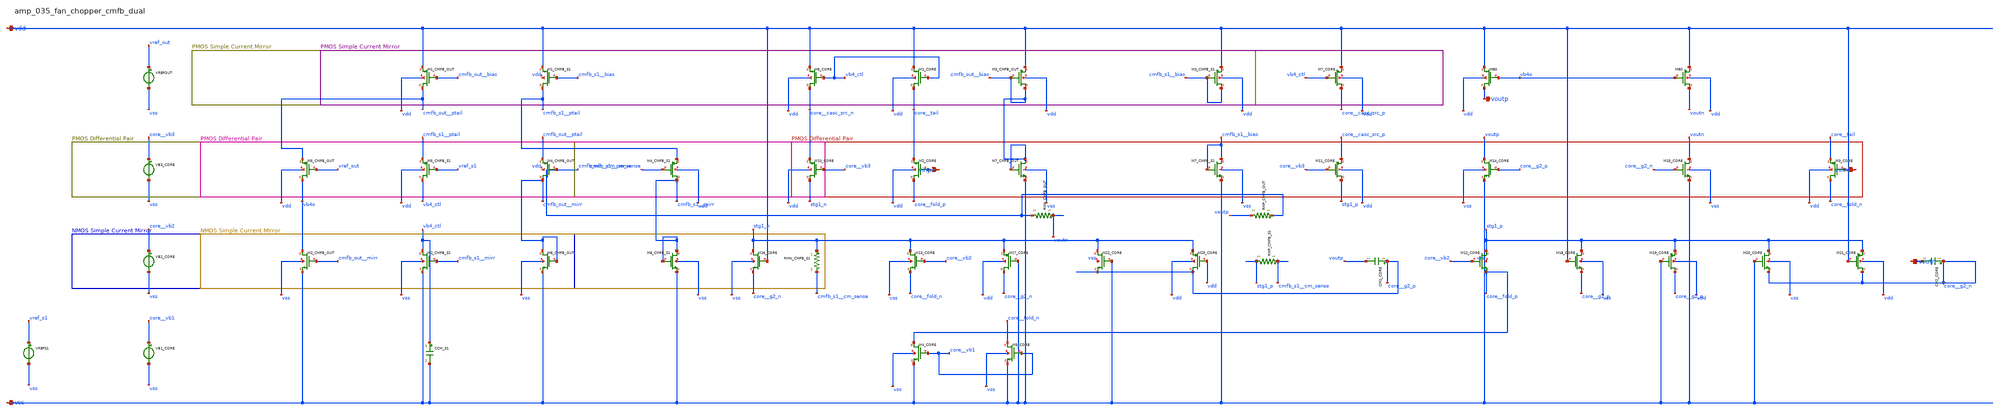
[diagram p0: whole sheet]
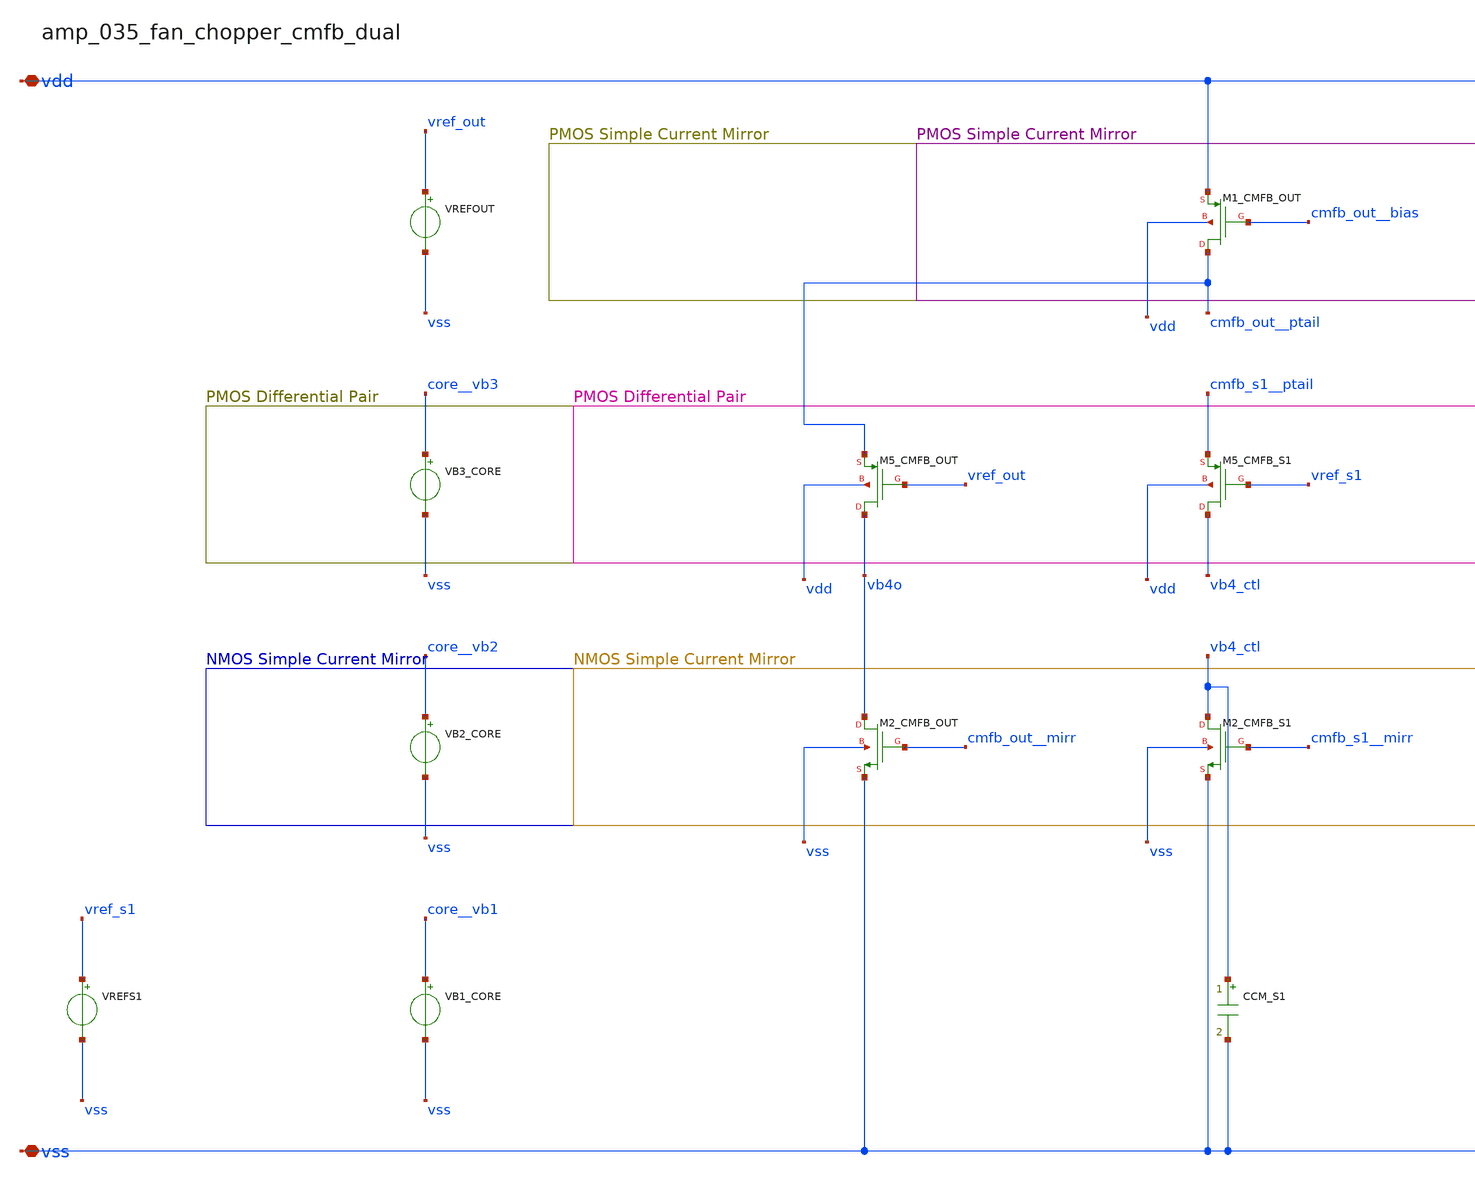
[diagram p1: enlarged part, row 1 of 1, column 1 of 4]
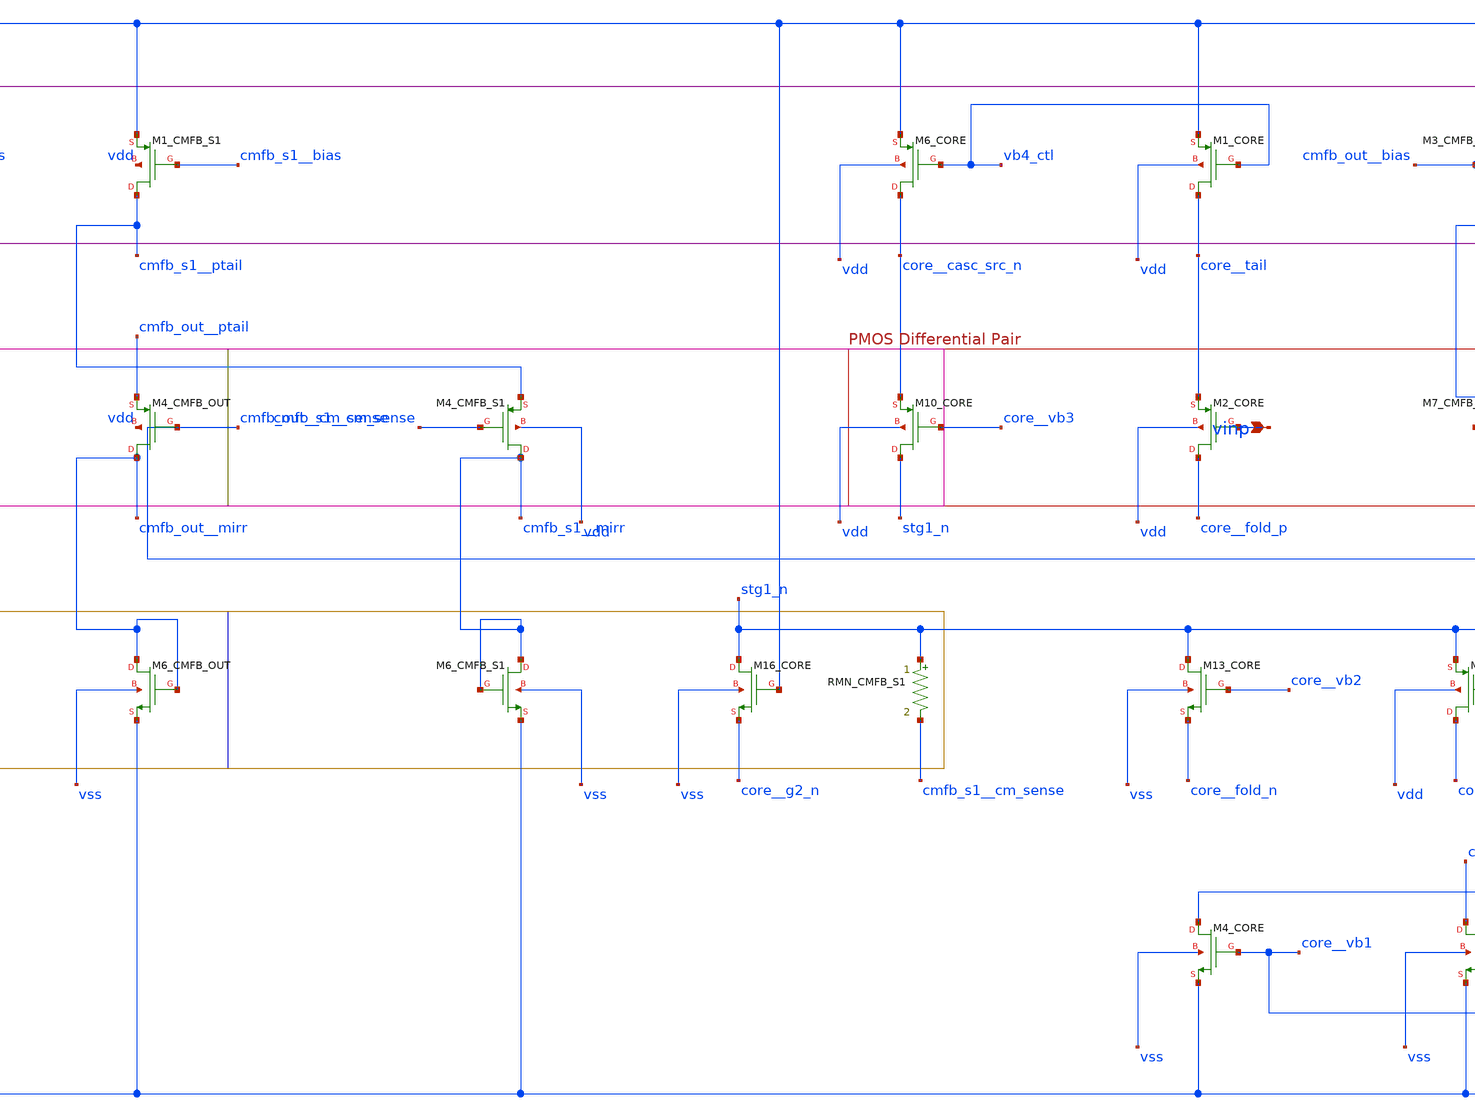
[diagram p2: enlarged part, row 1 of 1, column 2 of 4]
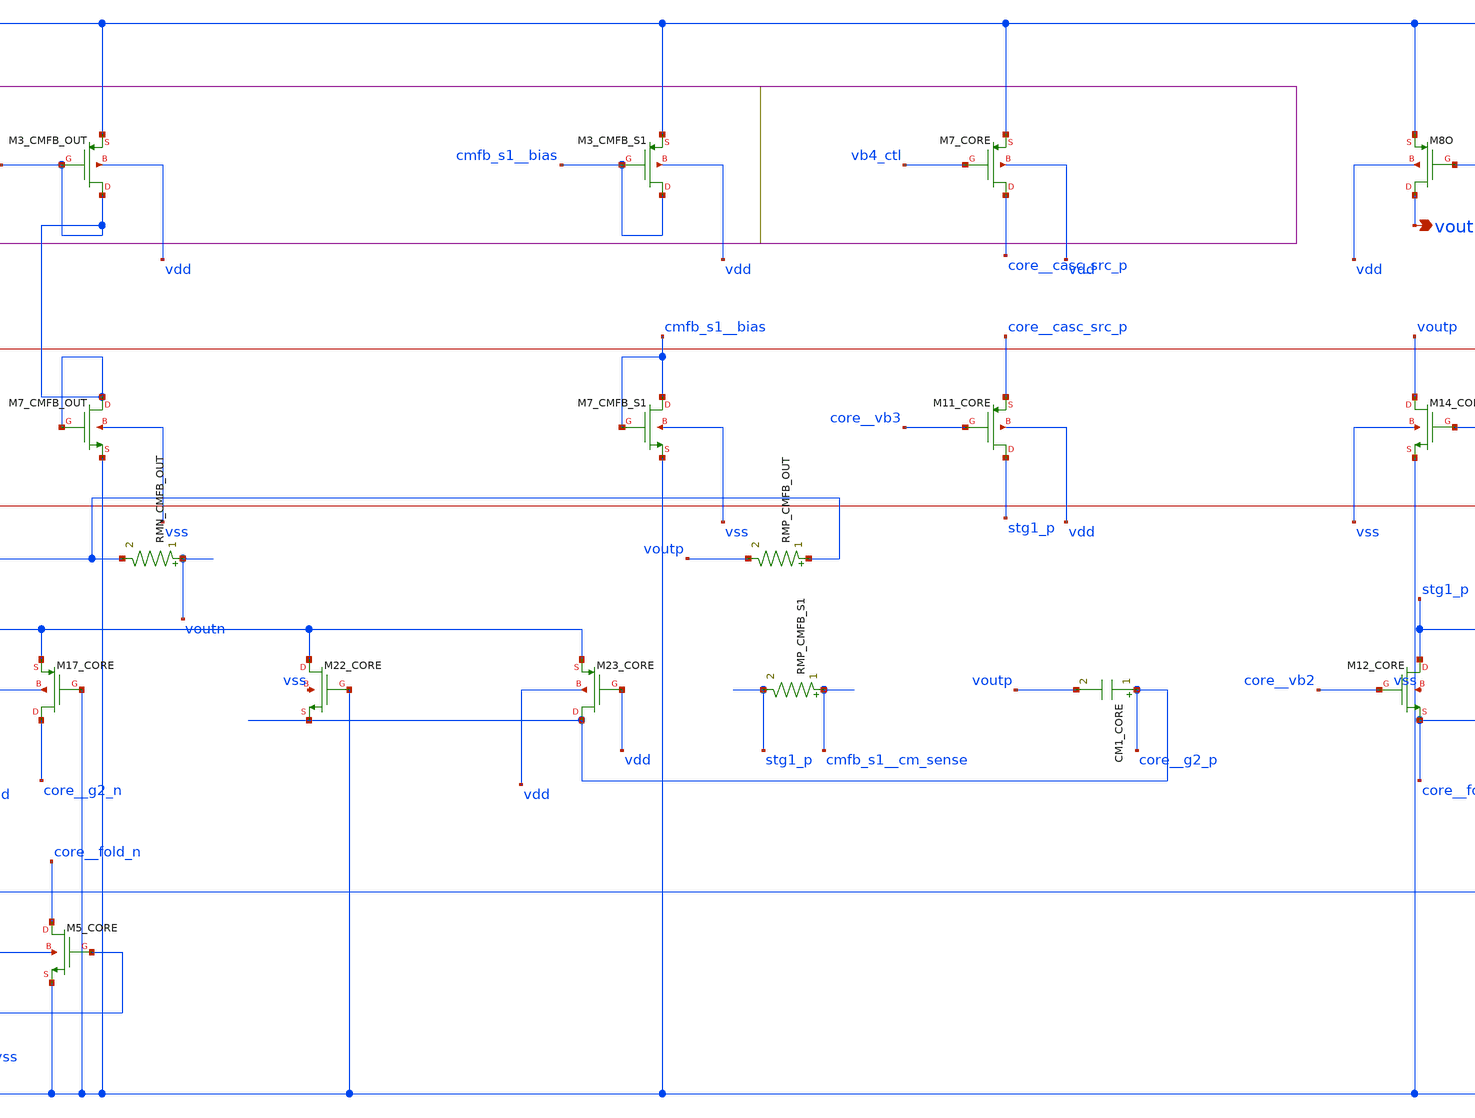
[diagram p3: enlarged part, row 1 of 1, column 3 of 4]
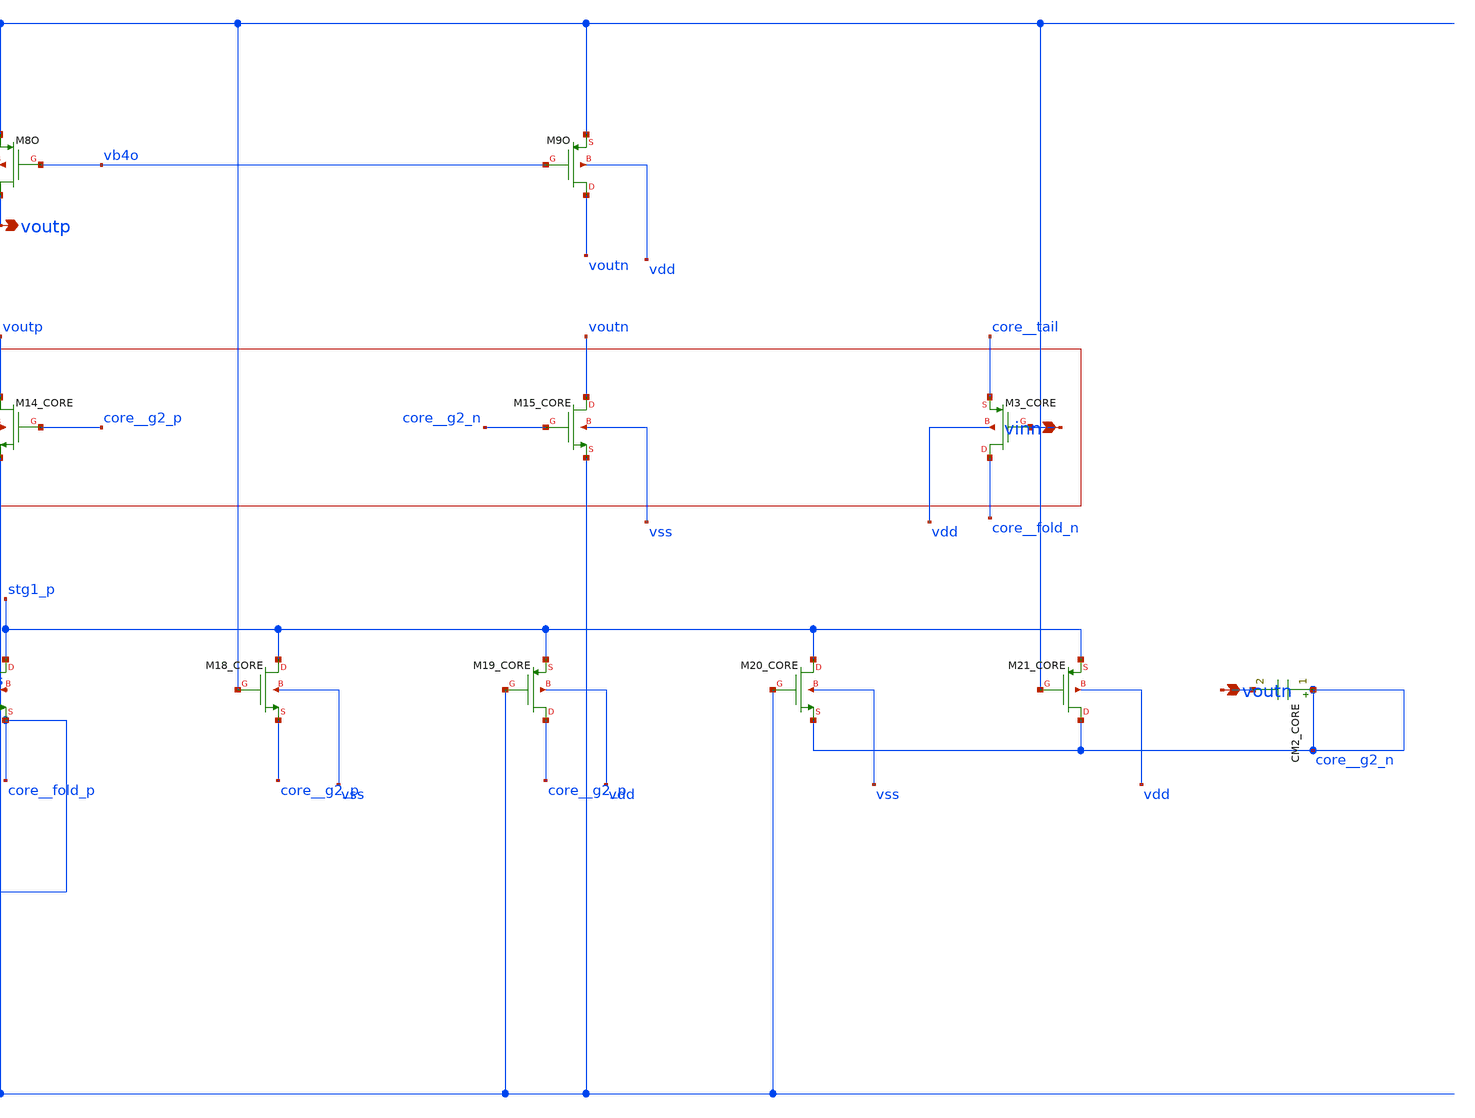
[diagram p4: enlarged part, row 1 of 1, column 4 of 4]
** sch_path: analog-db/raw/amp_035_fan_chopper_cmfb_dual/amp_035_fan_chopper_cmfb_dual_annotated.sch
**.subckt amp_035_fan_chopper_cmfb_dual_annotated vinp vinn vdd vss voutp voutn
*.ipin vinp
*.ipin vinn
*.iopin vdd
*.iopin vss
*.opin voutp
*.opin voutn
CCM_S1 vb4_ctl vss 'c_cm_s1' m=1
CM1_CORE core__g2_p voutp 'x_dut_cm1_core_value' m=1
CM2_CORE core__g2_n voutn 'x_dut_cm2_core_value' m=1
RMN_CMFB_OUT voutn cmfb_out__cm_sense 'x_dut_rmn_cmfb_out_value' m=1
RMN_CMFB_S1 stg1_n cmfb_s1__cm_sense 'x_dut_rmn_cmfb_s1_value' m=1
RMP_CMFB_OUT cmfb_out__cm_sense voutp 'x_dut_rmp_cmfb_out_value' m=1
RMP_CMFB_S1 cmfb_s1__cm_sense stg1_p 'x_dut_rmp_cmfb_s1_value' m=1
VB1_CORE core__vb1 vss dc {vb1_core}
VB2_CORE core__vb2 vss dc {vb2_core}
VB3_CORE core__vb3 vss dc {vb3_core}
VREFOUT vref_out vss dc {vcm_ref}
VREFS1 vref_s1 vss dc {vcm_ref_stg1}
XM10_CORE stg1_n core__vb3 core__casc_src_n vdd sg13_lv_pmos w=x_dut_xm10_core_w l=x_dut_xm10_core_l
+ ng=1 m=x_dut_xm10_core_m
XM11_CORE stg1_p core__vb3 core__casc_src_p vdd sg13_lv_pmos w=x_dut_xm11_core_w l=x_dut_xm11_core_l
+ ng=1 m=x_dut_xm11_core_m
XM12_CORE stg1_p core__vb2 core__fold_p vss sg13_lv_nmos w=x_dut_xm12_core_w l=x_dut_xm12_core_l
+ ng=1 m=x_dut_xm12_core_m
XM13_CORE stg1_n core__vb2 core__fold_n vss sg13_lv_nmos w=x_dut_xm13_core_w l=x_dut_xm13_core_l
+ ng=1 m=x_dut_xm13_core_m
XM14_CORE voutp core__g2_p vss vss sg13_lv_nmos w=x_dut_xm14_core_w l=x_dut_xm14_core_l ng=1
+ m=x_dut_xm14_core_m
XM15_CORE voutn core__g2_n vss vss sg13_lv_nmos w=x_dut_xm15_core_w l=x_dut_xm15_core_l ng=1
+ m=x_dut_xm15_core_m
XM16_CORE stg1_n vdd core__g2_n vss sg13_lv_nmos w=x_dut_xm16_core_w l=x_dut_xm16_core_l ng=1
+ m=x_dut_xm16_core_m
XM17_CORE core__g2_n vss stg1_n vdd sg13_lv_pmos w=x_dut_xm17_core_w l=x_dut_xm17_core_l ng=1
+ m=x_dut_xm17_core_m
XM18_CORE stg1_p vdd core__g2_p vss sg13_lv_nmos w=x_dut_xm18_core_w l=x_dut_xm18_core_l ng=1
+ m=x_dut_xm18_core_m
XM19_CORE core__g2_p vss stg1_p vdd sg13_lv_pmos w=x_dut_xm19_core_w l=x_dut_xm19_core_l ng=1
+ m=x_dut_xm19_core_m
XM1_CMFB_OUT cmfb_out__ptail cmfb_out__bias vdd vdd sg13_lv_pmos w=x_dut_xm1_cmfb_out_w
+ l=x_dut_xm1_cmfb_out_l ng=1 m=x_dut_xm1_cmfb_out_m
XM1_CMFB_S1 cmfb_s1__ptail cmfb_s1__bias vdd vdd sg13_lv_pmos w=x_dut_xm1_cmfb_s1_w
+ l=x_dut_xm1_cmfb_s1_l ng=1 m=x_dut_xm1_cmfb_s1_m
XM1_CORE core__tail vb4_ctl vdd vdd sg13_lv_pmos w=x_dut_xm1_core_w l=x_dut_xm1_core_l ng=1
+ m=x_dut_xm1_core_m
XM20_CORE stg1_p vss core__g2_n vss sg13_lv_nmos w=x_dut_xm20_core_w l=x_dut_xm20_core_l ng=1
+ m=x_dut_xm20_core_m
XM21_CORE core__g2_n vdd stg1_p vdd sg13_lv_pmos w=x_dut_xm21_core_w l=x_dut_xm21_core_l ng=1
+ m=x_dut_xm21_core_m
XM22_CORE stg1_n vss core__g2_p vss sg13_lv_nmos w=x_dut_xm22_core_w l=x_dut_xm22_core_l ng=1
+ m=x_dut_xm22_core_m
XM23_CORE core__g2_p vdd stg1_n vdd sg13_lv_pmos w=x_dut_xm23_core_w l=x_dut_xm23_core_l ng=1
+ m=x_dut_xm23_core_m
XM2_CMFB_OUT vb4o cmfb_out__mirr vss vss sg13_lv_nmos w=x_dut_xm2_cmfb_out_w l=x_dut_xm2_cmfb_out_l
+ ng=1 m=x_dut_xm2_cmfb_out_m
XM2_CMFB_S1 vb4_ctl cmfb_s1__mirr vss vss sg13_lv_nmos w=x_dut_xm2_cmfb_s1_w l=x_dut_xm2_cmfb_s1_l
+ ng=1 m=x_dut_xm2_cmfb_s1_m
XM2_CORE core__fold_p vinp core__tail vdd sg13_lv_pmos w=x_dut_xm2_core_w l=x_dut_xm2_core_l ng=1
+ m=x_dut_xm2_core_m
XM3_CMFB_OUT cmfb_out__bias cmfb_out__bias vdd vdd sg13_lv_pmos w=x_dut_xm3_cmfb_out_w
+ l=x_dut_xm3_cmfb_out_l ng=1 m=x_dut_xm3_cmfb_out_m
XM3_CMFB_S1 cmfb_s1__bias cmfb_s1__bias vdd vdd sg13_lv_pmos w=x_dut_xm3_cmfb_s1_w
+ l=x_dut_xm3_cmfb_s1_l ng=1 m=x_dut_xm3_cmfb_s1_m
XM3_CORE core__fold_n vinn core__tail vdd sg13_lv_pmos w=x_dut_xm3_core_w l=x_dut_xm3_core_l ng=1
+ m=x_dut_xm3_core_m
XM4_CMFB_OUT cmfb_out__mirr cmfb_out__cm_sense cmfb_out__ptail vdd sg13_lv_pmos
+ w=x_dut_xm4_cmfb_out_w l=x_dut_xm4_cmfb_out_l ng=1 m=x_dut_xm4_cmfb_out_m
XM4_CMFB_S1 cmfb_s1__mirr cmfb_s1__cm_sense cmfb_s1__ptail vdd sg13_lv_pmos w=x_dut_xm4_cmfb_s1_w
+ l=x_dut_xm4_cmfb_s1_l ng=1 m=x_dut_xm4_cmfb_s1_m
XM4_CORE core__fold_p core__vb1 vss vss sg13_lv_nmos w=x_dut_xm4_core_w l=x_dut_xm4_core_l ng=1
+ m=x_dut_xm4_core_m
XM5_CMFB_OUT vb4o vref_out cmfb_out__ptail vdd sg13_lv_pmos w=x_dut_xm5_cmfb_out_w
+ l=x_dut_xm5_cmfb_out_l ng=1 m=x_dut_xm5_cmfb_out_m
XM5_CMFB_S1 vb4_ctl vref_s1 cmfb_s1__ptail vdd sg13_lv_pmos w=x_dut_xm5_cmfb_s1_w
+ l=x_dut_xm5_cmfb_s1_l ng=1 m=x_dut_xm5_cmfb_s1_m
XM5_CORE core__fold_n core__vb1 vss vss sg13_lv_nmos w=x_dut_xm5_core_w l=x_dut_xm5_core_l ng=1
+ m=x_dut_xm5_core_m
XM6_CMFB_OUT cmfb_out__mirr cmfb_out__mirr vss vss sg13_lv_nmos w=x_dut_xm6_cmfb_out_w
+ l=x_dut_xm6_cmfb_out_l ng=1 m=x_dut_xm6_cmfb_out_m
XM6_CMFB_S1 cmfb_s1__mirr cmfb_s1__mirr vss vss sg13_lv_nmos w=x_dut_xm6_cmfb_s1_w
+ l=x_dut_xm6_cmfb_s1_l ng=1 m=x_dut_xm6_cmfb_s1_m
XM6_CORE core__casc_src_n vb4_ctl vdd vdd sg13_lv_pmos w=x_dut_xm6_core_w l=x_dut_xm6_core_l ng=1
+ m=x_dut_xm6_core_m
XM7_CMFB_OUT cmfb_out__bias cmfb_out__bias vss vss sg13_lv_nmos w=x_dut_xm7_cmfb_out_w
+ l=x_dut_xm7_cmfb_out_l ng=1 m=x_dut_xm7_cmfb_out_m
XM7_CMFB_S1 cmfb_s1__bias cmfb_s1__bias vss vss sg13_lv_nmos w=x_dut_xm7_cmfb_s1_w
+ l=x_dut_xm7_cmfb_s1_l ng=1 m=x_dut_xm7_cmfb_s1_m
XM7_CORE core__casc_src_p vb4_ctl vdd vdd sg13_lv_pmos w=x_dut_xm7_core_w l=x_dut_xm7_core_l ng=1
+ m=x_dut_xm7_core_m
XM8O voutp vb4o vdd vdd sg13_lv_pmos w=x_dut_xm8o_w l=x_dut_xm8o_l ng=1 m=x_dut_xm8o_m
XM9O voutn vb4o vdd vdd sg13_lv_pmos w=x_dut_xm9o_w l=x_dut_xm9o_l ng=1 m=x_dut_xm9o_m
**.ends
.end
